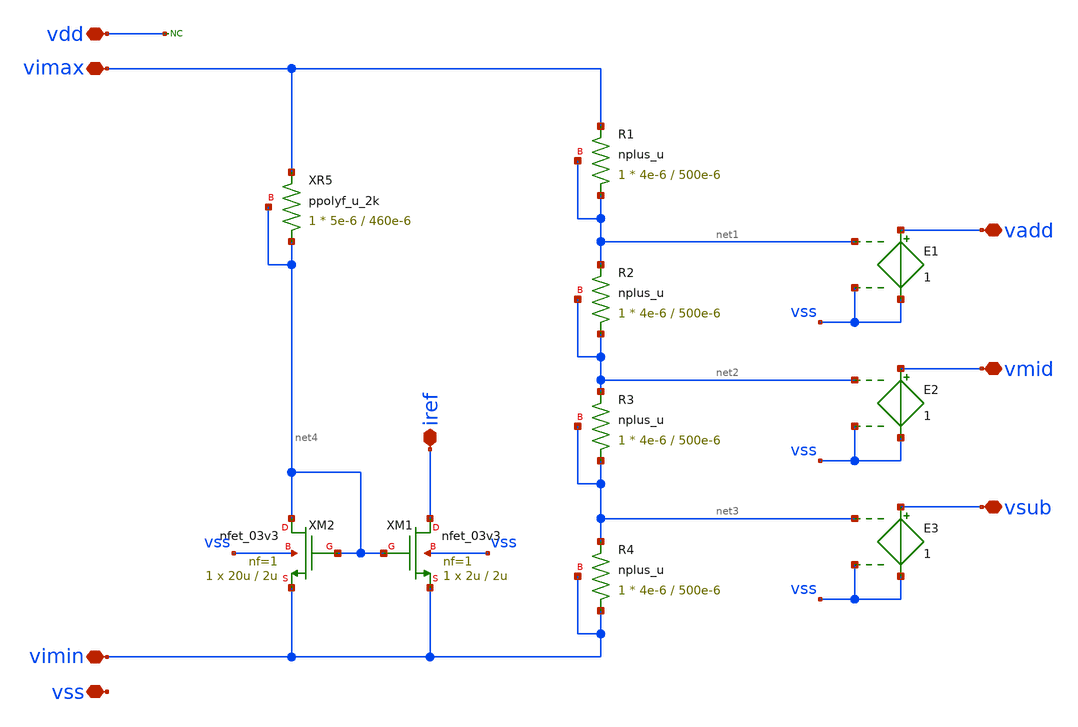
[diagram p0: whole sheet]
** sch_path: General/ADC/Reference/Reference_circuits_v2.sch
**.subckt Reference_circuits_v2 vimax vimin iref vadd vmid vsub vss vdd
*.iopin vimax
*.iopin vimin
*.iopin iref
*.iopin vadd
*.iopin vmid
*.iopin vsub
*.iopin vss
*.iopin vdd
XR1 net1 vimax net1 nplus_u r_width=4e-6 r_length=500e-6 m=1
XR2 net2 net1 net2 nplus_u r_width=4e-6 r_length=500e-6 m=1
XR3 net3 net2 net3 nplus_u r_width=4e-6 r_length=500e-6 m=1
XR4 vimin net3 vimin nplus_u r_width=4e-6 r_length=500e-6 m=1
XM2 net4 net4 vimin vss nfet_03v3 L=2u W=20u nf=1 ad='int((nf+1)/2) * W/nf * 0.18u' as='int((nf+2)/2) * W/nf * 0.18u'
+ pd='2*int((nf+1)/2) * (W/nf + 0.18u)' ps='2*int((nf+2)/2) * (W/nf + 0.18u)' nrd='0.18u / W' nrs='0.18u / W'
+ sa=0 sb=0 sd=0 m=1
XR5 net4 vimax net4 ppolyf_u_2k r_width=5e-6 r_length=460e-6 m=1
XM1 iref net4 vimin vss nfet_03v3 L=2u W=2u nf=1 ad='int((nf+1)/2) * W/nf * 0.18u' as='int((nf+2)/2) * W/nf * 0.18u'
+ pd='2*int((nf+1)/2) * (W/nf + 0.18u)' ps='2*int((nf+2)/2) * (W/nf + 0.18u)' nrd='0.18u / W' nrs='0.18u / W'
+ sa=0 sb=0 sd=0 m=1
* noconn vdd
E1 vadd vss net1 vss 1
E2 vmid vss net2 vss 1
E3 vsub vss net3 vss 1
**.ends
.end
